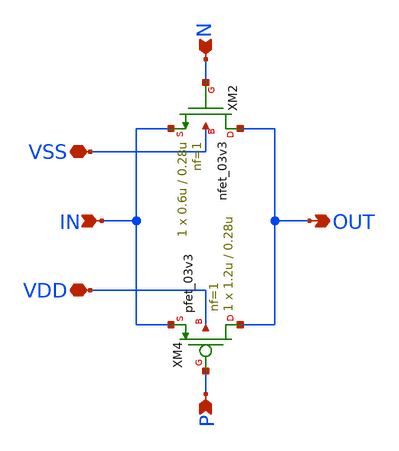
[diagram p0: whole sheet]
** sch_path: xschem/io_xfer_1.sch
* Copyright 2023 David Mitchell Bailey
* Licensed under the Apache License, Version 2.0 (the "License");
* you may not use this file except in compliance with the License.
* You may obtain a copy of the License at
* https://www.apache.org/licenses/LICENSE-2.0
* Unless required by applicable law or agreed to in writing, software
* distributed under the License is distributed on an "AS IS" BASIS,
* WITHOUT WARRANTIES OR CONDITIONS OF ANY KIND, either express or implied.
* See the License for the specific language governing permissions and
* limitations under the License.
**.subckt io_xfer_1 OUT IN N P VDD VSS
*.opin OUT
*.ipin IN
*.ipin N
*.ipin P
*.iopin VDD
*.iopin VSS
XM2 OUT N IN VSS nfet_03v3 L=0.28u W=0.6u nf=1 ad='int((nf+1)/2) * W/nf * 0.18u' as='int((nf+2)/2) * W/nf * 0.18u'
+ pd='2*int((nf+1)/2) * (W/nf + 0.18u)' ps='2*int((nf+2)/2) * (W/nf + 0.18u)' nrd='0.18u / W' nrs='0.18u / W'
+ sa=0 sb=0 sd=0 m=1 par=1
XM4 OUT P IN VDD pfet_03v3 L=0.28u W=1.2u nf=1 ad='int((nf+1)/2) * W/nf * 0.18u' as='int((nf+2)/2) * W/nf * 0.18u'
+ pd='2*int((nf+1)/2) * (W/nf + 0.18u)' ps='2*int((nf+2)/2) * (W/nf + 0.18u)' nrd='0.18u / W' nrs='0.18u / W'
+ sa=0 sb=0 sd=0 m=1 par=1
**.ends
.end
